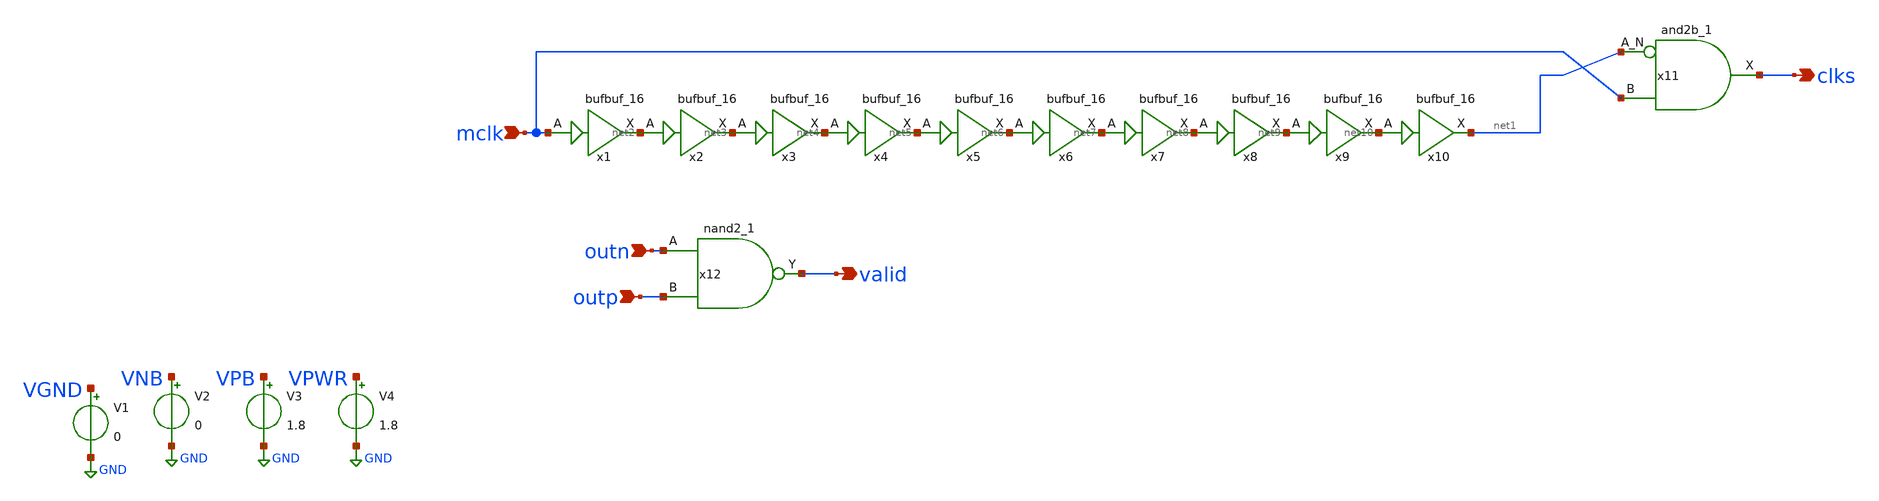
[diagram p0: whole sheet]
** sch_path: other_logic.sch
**.subckt other_logic mclk outn outp clks valid
*.ipin mclk
*.ipin outn
*.ipin outp
*.opin clks
*.opin valid
V1 VGND GND 0
V2 VNB GND 0
V3 VPB GND 1.8
V4 VPWR GND 1.8
x1 mclk VGND VNB VPB VPWR net2 sky130_fd_sc_hd__bufbuf_16
x2 net2 VGND VNB VPB VPWR net3 sky130_fd_sc_hd__bufbuf_16
x3 net3 VGND VNB VPB VPWR net4 sky130_fd_sc_hd__bufbuf_16
x4 net4 VGND VNB VPB VPWR net5 sky130_fd_sc_hd__bufbuf_16
x5 net5 VGND VNB VPB VPWR net6 sky130_fd_sc_hd__bufbuf_16
x6 net6 VGND VNB VPB VPWR net7 sky130_fd_sc_hd__bufbuf_16
x7 net7 VGND VNB VPB VPWR net8 sky130_fd_sc_hd__bufbuf_16
x8 net8 VGND VNB VPB VPWR net9 sky130_fd_sc_hd__bufbuf_16
x9 net9 VGND VNB VPB VPWR net10 sky130_fd_sc_hd__bufbuf_16
x10 net10 VGND VNB VPB VPWR net1 sky130_fd_sc_hd__bufbuf_16
x11 net1 mclk VGND VNB VPB VPWR clks sky130_fd_sc_hd__and2b_1
x12 outn outp VGND VNB VPB VPWR valid sky130_fd_sc_hd__nand2_1
**** begin user architecture code


.lib ~/open_pdks/sky130/sky130A/libs.tech/ngspice/sky130.lib.spice tt
.include ~/open_pdks/sky130/sky130A/libs.ref/sky130_fd_sc_hd/spice/sky130_fd_sc_hd.spice

**** end user architecture code
**.ends
.GLOBAL GND
.end
